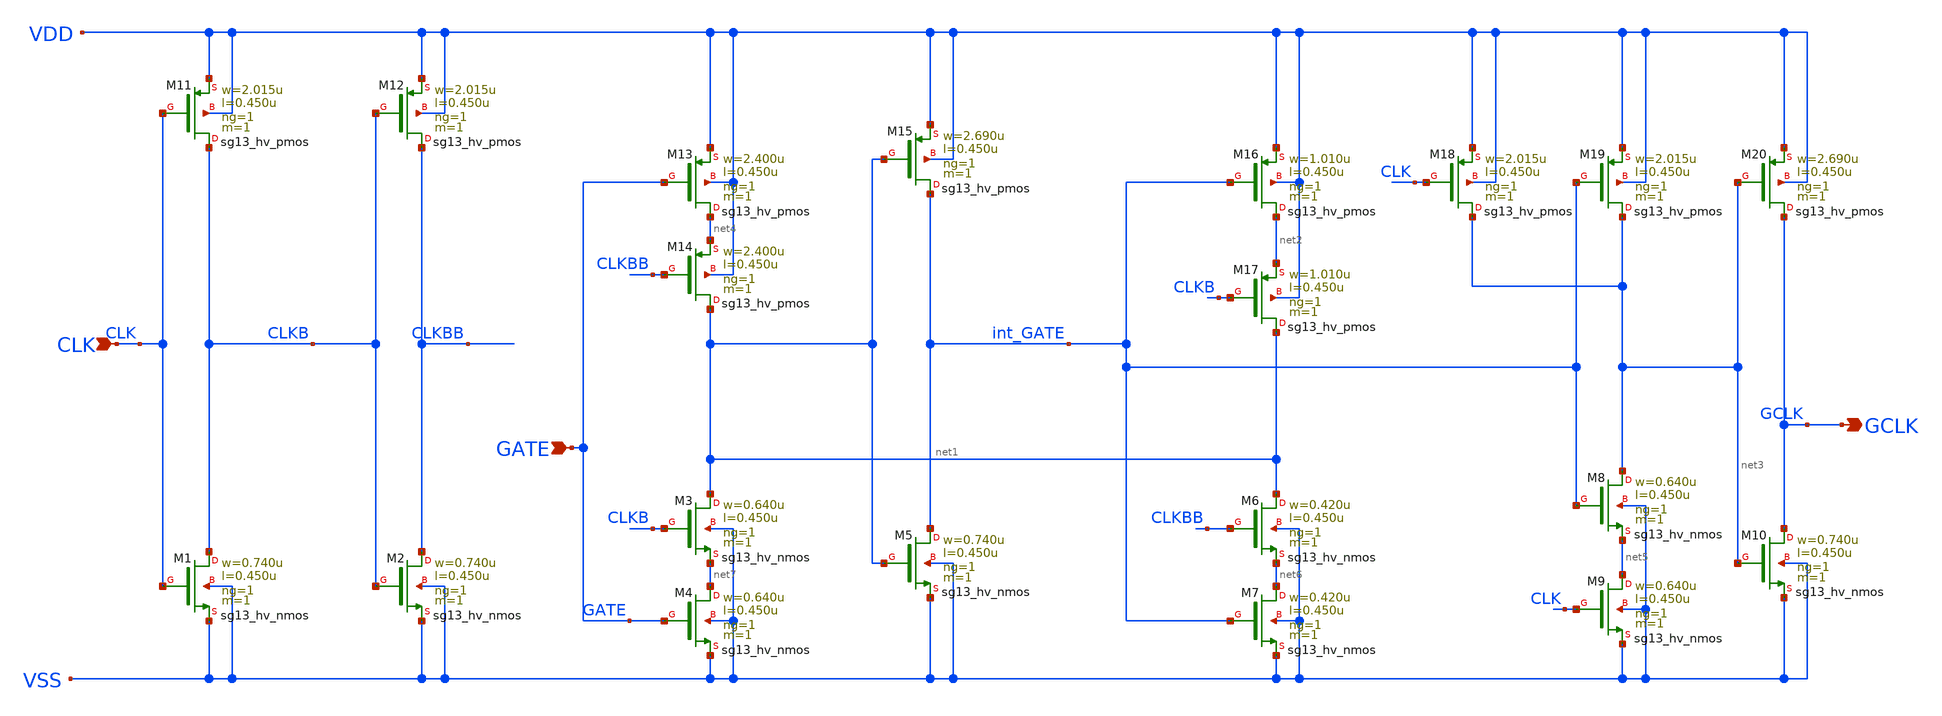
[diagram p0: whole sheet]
** sch_path: ihp-sg13g2/libs.ref/sg13g2_stdcell_hv/sch/xschem/sg13g2_hv_lgcp_1.sch
* Copyright 2023 IHP PDK Authors
* Licensed under the Apache License, Version 2.0 (the "License");
* you may not use this file except in compliance with the License.
* You may obtain a copy of the License at
* https://www.apache.org/licenses/LICENSE-2.0
* Unless required by applicable law or agreed to in writing, software
* distributed under the License is distributed on an "AS IS" BASIS,
* WITHOUT WARRANTIES OR CONDITIONS OF ANY KIND, either express or implied.
* See the License for the specific language governing permissions and
* limitations under the License.
**.subckt sg13g2_hv_lgcp_1 GCLK GATE CLK
*.opin GCLK
*.ipin GATE
*.ipin CLK
XM1 CLKB CLK VSS VSS sg13_hv_nmos w=0.740u l=0.450u ng=1 m=1 mm_ok=1
XM2 CLKBB CLKB VSS VSS sg13_hv_nmos w=0.740u l=0.450u ng=1 m=1 mm_ok=1
XM3 net1 CLKB net7 VSS sg13_hv_nmos w=0.640u l=0.450u ng=1 m=1 mm_ok=1
XM4 net7 GATE VSS VSS sg13_hv_nmos w=0.640u l=0.450u ng=1 m=1 mm_ok=1
XM5 int_GATE net1 VSS VSS sg13_hv_nmos w=0.740u l=0.450u ng=1 m=1 mm_ok=1
XM6 net1 CLKBB net6 VSS sg13_hv_nmos w=0.420u l=0.450u ng=1 m=1 mm_ok=1
XM7 net6 int_GATE VSS VSS sg13_hv_nmos w=0.420u l=0.450u ng=1 m=1 mm_ok=1
XM8 net3 int_GATE net5 VSS sg13_hv_nmos w=0.640u l=0.450u ng=1 m=1 mm_ok=1
XM9 net5 CLK VSS VSS sg13_hv_nmos w=0.640u l=0.450u ng=1 m=1 mm_ok=1
XM10 GCLK net3 VSS VSS sg13_hv_nmos w=0.740u l=0.450u ng=1 m=1 mm_ok=1
XM11 CLKB CLK VDD VDD sg13_hv_pmos w=2.015u l=0.450u ng=1 m=1 mm_ok=1
XM12 CLKBB CLKB VDD VDD sg13_hv_pmos w=2.015u l=0.450u ng=1 m=1 mm_ok=1
XM13 net4 GATE VDD VDD sg13_hv_pmos w=2.400u l=0.450u ng=1 m=1 mm_ok=1
XM14 net1 CLKBB net4 VDD sg13_hv_pmos w=2.400u l=0.450u ng=1 m=1 mm_ok=1
XM15 int_GATE net1 VDD VDD sg13_hv_pmos w=2.690u l=0.450u ng=1 m=1 mm_ok=1
XM16 net2 int_GATE VDD VDD sg13_hv_pmos w=1.010u l=0.450u ng=1 m=1 mm_ok=1
XM17 net1 CLKB net2 VDD sg13_hv_pmos w=1.010u l=0.450u ng=1 m=1 mm_ok=1
XM18 net3 CLK VDD VDD sg13_hv_pmos w=2.015u l=0.450u ng=1 m=1 mm_ok=1
XM19 net3 int_GATE VDD VDD sg13_hv_pmos w=2.015u l=0.450u ng=1 m=1 mm_ok=1
XM20 GCLK net3 VDD VDD sg13_hv_pmos w=2.690u l=0.450u ng=1 m=1 mm_ok=1
**.ends
.end
